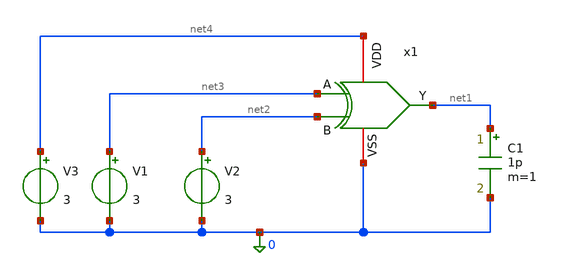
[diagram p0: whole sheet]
** sch_path: src/UN_PFD_GF180mcuD/work/untitled.sch
* src/UN_PFD_GF180mcuD/work/UN_xor_0_gf180mcuD.sch:
* Copyright (C) 1998-2024 Stefan Frederik Schippers
* This program is free software; you can redistribute it and/or modify
* it under the terms of the GNU General Public License as published by
* the Free Software Foundation; either version 2 of the License, or
* (at your option) any later version.
**.subckt untitled
V1 net3 0 3
V2 net2 0 3
x1 net4 net3 net1 net2 0 UN_xor_0_gf180mcuD
C1 net1 0 1p m=1
V3 net4 0 3
**.ends

* expanding   symbol:  UN_xor_0_gf180mcuD.sym # of pins=5
** sym_path: src/UN_PFD_GF180mcuD/work/UN_xor_0_gf180mcuD.sym
** sch_path: src/UN_PFD_GF180mcuD/work/UN_xor_0_gf180mcuD.sch
.subckt UN_xor_0_gf180mcuD VDD A Y B VSS
*.iopin VSS
*.iopin VDD
*.opin Y
*.ipin A
*.ipin B
XM1 Y A_n net2 VSS nfet_03v3 L=0.28u W=0.5u nf=1 ad='int((nf+1)/2) * W/nf * 0.18u' as='int((nf+2)/2) * W/nf * 0.18u'
+ pd='2*int((nf+1)/2) * (W/nf + 0.18u)' ps='2*int((nf+2)/2) * (W/nf + 0.18u)' nrd='0.18u / W' nrs='0.18u / W'
+ sa=0 sb=0 sd=0 m=1
XM2 Y A net1 VSS nfet_03v3 L=0.28u W=0.5u nf=1 ad='int((nf+1)/2) * W/nf * 0.18u' as='int((nf+2)/2) * W/nf * 0.18u'
+ pd='2*int((nf+1)/2) * (W/nf + 0.18u)' ps='2*int((nf+2)/2) * (W/nf + 0.18u)' nrd='0.18u / W' nrs='0.18u / W'
+ sa=0 sb=0 sd=0 m=1
XM3 net2 B_n VSS VSS nfet_03v3 L=0.28u W=0.5u nf=1 ad='int((nf+1)/2) * W/nf * 0.18u' as='int((nf+2)/2) * W/nf * 0.18u'
+ pd='2*int((nf+1)/2) * (W/nf + 0.18u)' ps='2*int((nf+2)/2) * (W/nf + 0.18u)' nrd='0.18u / W' nrs='0.18u / W'
+ sa=0 sb=0 sd=0 m=1
XM4 net1 B VSS VSS nfet_03v3 L=0.28u W=0.5u nf=1 ad='int((nf+1)/2) * W/nf * 0.18u' as='int((nf+2)/2) * W/nf * 0.18u'
+ pd='2*int((nf+1)/2) * (W/nf + 0.18u)' ps='2*int((nf+2)/2) * (W/nf + 0.18u)' nrd='0.18u / W' nrs='0.18u / W'
+ sa=0 sb=0 sd=0 m=1
XM5 Y A_n net3 VDD pfet_03v3 L=0.28u W=1u nf=1 ad='int((nf+1)/2) * W/nf * 0.18u' as='int((nf+2)/2) * W/nf * 0.18u'
+ pd='2*int((nf+1)/2) * (W/nf + 0.18u)' ps='2*int((nf+2)/2) * (W/nf + 0.18u)' nrd='0.18u / W' nrs='0.18u / W'
+ sa=0 sb=0 sd=0 m=1
XM6 net3 A VDD VDD pfet_03v3 L=0.28u W=1u nf=1 ad='int((nf+1)/2) * W/nf * 0.18u' as='int((nf+2)/2) * W/nf * 0.18u'
+ pd='2*int((nf+1)/2) * (W/nf + 0.18u)' ps='2*int((nf+2)/2) * (W/nf + 0.18u)' nrd='0.18u / W' nrs='0.18u / W'
+ sa=0 sb=0 sd=0 m=1
XM7 Y B_n net4 VDD pfet_03v3 L=0.28u W=1u nf=1 ad='int((nf+1)/2) * W/nf * 0.18u' as='int((nf+2)/2) * W/nf * 0.18u'
+ pd='2*int((nf+1)/2) * (W/nf + 0.18u)' ps='2*int((nf+2)/2) * (W/nf + 0.18u)' nrd='0.18u / W' nrs='0.18u / W'
+ sa=0 sb=0 sd=0 m=1
XM8 net4 B VDD VDD pfet_03v3 L=0.28u W=1u nf=1 ad='int((nf+1)/2) * W/nf * 0.18u' as='int((nf+2)/2) * W/nf * 0.18u'
+ pd='2*int((nf+1)/2) * (W/nf + 0.18u)' ps='2*int((nf+2)/2) * (W/nf + 0.18u)' nrd='0.18u / W' nrs='0.18u / W'
+ sa=0 sb=0 sd=0 m=1
XM9 A_n A VDD VDD pfet_03v3 L=0.28u W=1u nf=1 ad='int((nf+1)/2) * W/nf * 0.18u' as='int((nf+2)/2) * W/nf * 0.18u'
+ pd='2*int((nf+1)/2) * (W/nf + 0.18u)' ps='2*int((nf+2)/2) * (W/nf + 0.18u)' nrd='0.18u / W' nrs='0.18u / W'
+ sa=0 sb=0 sd=0 m=1
XM10 A_n A VSS VSS nfet_03v3 L=0.28u W=0.5u nf=1 ad='int((nf+1)/2) * W/nf * 0.18u' as='int((nf+2)/2) * W/nf * 0.18u'
+ pd='2*int((nf+1)/2) * (W/nf + 0.18u)' ps='2*int((nf+2)/2) * (W/nf + 0.18u)' nrd='0.18u / W' nrs='0.18u / W'
+ sa=0 sb=0 sd=0 m=1
XM11 B_n B VDD VDD pfet_03v3 L=0.28u W=1u nf=1 ad='int((nf+1)/2) * W/nf * 0.18u' as='int((nf+2)/2) * W/nf * 0.18u'
+ pd='2*int((nf+1)/2) * (W/nf + 0.18u)' ps='2*int((nf+2)/2) * (W/nf + 0.18u)' nrd='0.18u / W' nrs='0.18u / W'
+ sa=0 sb=0 sd=0 m=1
XM12 B_n B VSS VSS nfet_03v3 L=0.28u W=0.5u nf=1 ad='int((nf+1)/2) * W/nf * 0.18u' as='int((nf+2)/2) * W/nf * 0.18u'
+ pd='2*int((nf+1)/2) * (W/nf + 0.18u)' ps='2*int((nf+2)/2) * (W/nf + 0.18u)' nrd='0.18u / W' nrs='0.18u / W'
+ sa=0 sb=0 sd=0 m=1
.ends

.end
